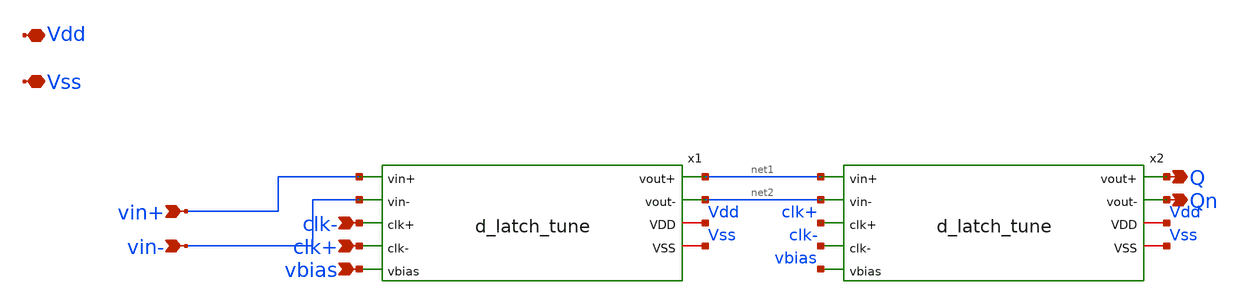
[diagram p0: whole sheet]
** sch_path: xschem/tuning/d_flip_flop_tune.sch
**.subckt d_flip_flop_tune Qn Q vin+ vin- clk+ clk- vbias Vdd Vss
*.opin Qn
*.opin Q
*.ipin vin+
*.ipin vin-
*.ipin clk+
*.ipin clk-
*.ipin vbias
*.iopin Vdd
*.iopin Vss
x1 net1 net2 vin+ vin- Vdd Vss clk- clk+ vbias d_latch_tune
x2 Q Qn net1 net2 Vdd Vss clk+ clk- vbias d_latch_tune
**.ends

* expanding   symbol:  d_latch_tune.sym # of pins=9
** sym_path: xschem/tuning/d_latch_tune.sym
** sch_path: xschem/tuning/d_latch_tune.sch
.subckt d_latch_tune vout+ vout- vin+ vin- VDD VSS clk+ clk- vbias
*.iopin VDD
*.iopin VSS
*.ipin vin+
*.ipin clk-
*.ipin vbias
*.opin vout+
*.ipin clk+
*.opin vout-
*.ipin vin-
XM1 net1 vin+ net3 VSS sky130_fd_pr__nfet_01v8 L=0.15 W=5 nf=1 ad='int((nf+1)/2) * W/nf * 0.29' as='int((nf+2)/2) * W/nf * 0.29'
+ pd='2*int((nf+1)/2) * (W/nf + 0.29)' ps='2*int((nf+2)/2) * (W/nf + 0.29)' nrd='0.29 / W' nrs='0.29 / W'
+ sa=0 sb=0 sd=0 mult=1 m=1
XM2 net4 vbias VSS VSS sky130_fd_pr__nfet_01v8 L=0.15 W=8 nf=1 ad='int((nf+1)/2) * W/nf * 0.29' as='int((nf+2)/2) * W/nf * 0.29'
+ pd='2*int((nf+1)/2) * (W/nf + 0.29)' ps='2*int((nf+2)/2) * (W/nf + 0.29)' nrd='0.29 / W' nrs='0.29 / W'
+ sa=0 sb=0 sd=0 mult=1 m=1
XM4 net2 vin- net3 VSS sky130_fd_pr__nfet_01v8 L=0.15 W=5 nf=1 ad='int((nf+1)/2) * W/nf * 0.29' as='int((nf+2)/2) * W/nf * 0.29'
+ pd='2*int((nf+1)/2) * (W/nf + 0.29)' ps='2*int((nf+2)/2) * (W/nf + 0.29)' nrd='0.29 / W' nrs='0.29 / W'
+ sa=0 sb=0 sd=0 mult=1 m=1
XM3 net2 net1 net5 VSS sky130_fd_pr__nfet_01v8 L=0.15 W=5 nf=1 ad='int((nf+1)/2) * W/nf * 0.29' as='int((nf+2)/2) * W/nf * 0.29'
+ pd='2*int((nf+1)/2) * (W/nf + 0.29)' ps='2*int((nf+2)/2) * (W/nf + 0.29)' nrd='0.29 / W' nrs='0.29 / W'
+ sa=0 sb=0 sd=0 mult=1 m=1
XM5 net1 net2 net5 VSS sky130_fd_pr__nfet_01v8 L=0.15 W=5 nf=1 ad='int((nf+1)/2) * W/nf * 0.29' as='int((nf+2)/2) * W/nf * 0.29'
+ pd='2*int((nf+1)/2) * (W/nf + 0.29)' ps='2*int((nf+2)/2) * (W/nf + 0.29)' nrd='0.29 / W' nrs='0.29 / W'
+ sa=0 sb=0 sd=0 mult=1 m=1
XM6 net3 clk+ net4 VSS sky130_fd_pr__nfet_01v8 L=0.15 W=5 nf=1 ad='int((nf+1)/2) * W/nf * 0.29' as='int((nf+2)/2) * W/nf * 0.29'
+ pd='2*int((nf+1)/2) * (W/nf + 0.29)' ps='2*int((nf+2)/2) * (W/nf + 0.29)' nrd='0.29 / W' nrs='0.29 / W'
+ sa=0 sb=0 sd=0 mult=1 m=1
XM7 net5 clk- net4 VSS sky130_fd_pr__nfet_01v8 L=0.15 W=5 nf=1 ad='int((nf+1)/2) * W/nf * 0.29' as='int((nf+2)/2) * W/nf * 0.29'
+ pd='2*int((nf+1)/2) * (W/nf + 0.29)' ps='2*int((nf+2)/2) * (W/nf + 0.29)' nrd='0.29 / W' nrs='0.29 / W'
+ sa=0 sb=0 sd=0 mult=1 m=1
XM8 vout+ net1 VDD VDD sky130_fd_pr__pfet_01v8 L=0.15 W=3 nf=1 ad='int((nf+1)/2) * W/nf * 0.29' as='int((nf+2)/2) * W/nf * 0.29'
+ pd='2*int((nf+1)/2) * (W/nf + 0.29)' ps='2*int((nf+2)/2) * (W/nf + 0.29)' nrd='0.29 / W' nrs='0.29 / W'
+ sa=0 sb=0 sd=0 mult=1 m=1
XM9 vout+ net1 VSS VSS sky130_fd_pr__nfet_01v8 L=0.15 W=1 nf=1 ad='int((nf+1)/2) * W/nf * 0.29' as='int((nf+2)/2) * W/nf * 0.29'
+ pd='2*int((nf+1)/2) * (W/nf + 0.29)' ps='2*int((nf+2)/2) * (W/nf + 0.29)' nrd='0.29 / W' nrs='0.29 / W'
+ sa=0 sb=0 sd=0 mult=1 m=1
XM10 vout- net2 VDD VDD sky130_fd_pr__pfet_01v8 L=0.15 W=3 nf=1 ad='int((nf+1)/2) * W/nf * 0.29' as='int((nf+2)/2) * W/nf * 0.29'
+ pd='2*int((nf+1)/2) * (W/nf + 0.29)' ps='2*int((nf+2)/2) * (W/nf + 0.29)' nrd='0.29 / W' nrs='0.29 / W'
+ sa=0 sb=0 sd=0 mult=1 m=1
XM11 vout- net2 VSS VSS sky130_fd_pr__nfet_01v8 L=0.15 W=1 nf=1 ad='int((nf+1)/2) * W/nf * 0.29' as='int((nf+2)/2) * W/nf * 0.29'
+ pd='2*int((nf+1)/2) * (W/nf + 0.29)' ps='2*int((nf+2)/2) * (W/nf + 0.29)' nrd='0.29 / W' nrs='0.29 / W'
+ sa=0 sb=0 sd=0 mult=1 m=1
XR3 net1 VDD VSS sky130_fd_pr__res_high_po_0p69 L=7 mult=1 m=1
XR1 net2 VDD VSS sky130_fd_pr__res_high_po_0p69 L=7 mult=1 m=1
.ends

.end
